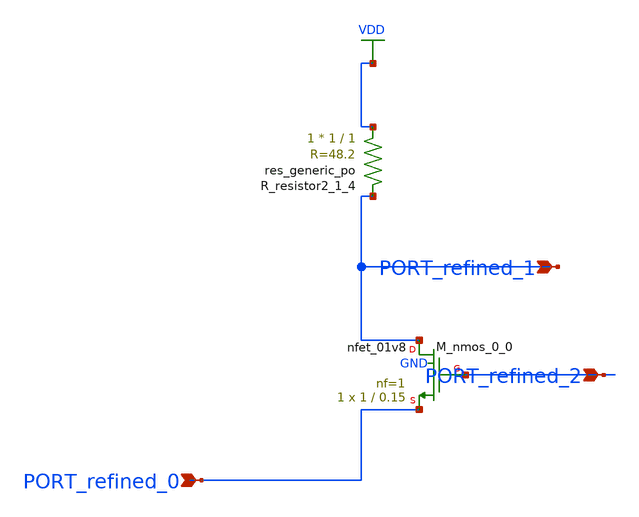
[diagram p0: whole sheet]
** sch_path: schematics/AMSNet/547.sch
**.subckt 547 PORT_refined_2 PORT_refined_1 PORT_refined_0
*.ipin PORT_refined_2
*.ipin PORT_refined_1
*.ipin PORT_refined_0
XM_nmos_0_0 PORT_refined_1 PORT_refined_2 PORT_refined_0 GND sky130_fd_pr__nfet_01v8 L=0.15 W=1 nf=1
+ ad='int((1 + 1)/2) * 1 / 1 * 0.29' as='int((1 + 2)/2) * 1 / 1 * 0.29' pd='2*int((1 + 1)/2) * (1 / 1 + 0.29)'
+ ps='2*int((1 + 2)/2) * (1 / 1 + 0.29)' nrd='0.29 / 1 ' nrs='0.29 / 1 ' sa=0 sb=0 sd=0 mult=1 m=1
XR_resistor2_1_4 VDD PORT_refined_1 sky130_fd_pr__res_generic_po W=1 L=1 m=1
**.ends
.GLOBAL VDD
.end
